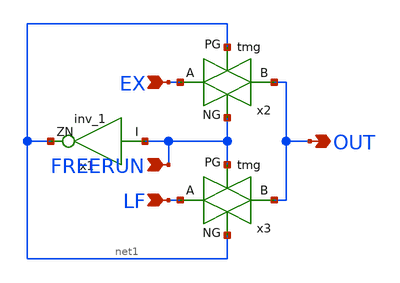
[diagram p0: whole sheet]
** sch_path: ctrlsel.sch
**.subckt ctrlsel OUT EX LF FREERUN
*.opin OUT
*.ipin EX
*.ipin LF
*.ipin FREERUN
x1 FREERUN net1 VDD VDD GND GND gf180mcu_fd_sc_mcu7t5v0__inv_1
x2 net1 OUT EX FREERUN tmg
x3 FREERUN OUT LF net1 tmg
**.ends

* expanding   symbol:  tmg.sym # of pins=4
** sym_path: tmg.sym
** sch_path: tmg.sch
.subckt tmg PG B A NG
*.opin B
*.ipin A
*.ipin PG
*.ipin NG
XM1 B NG A GND nfet_06v0 L=0.70u W=0.30u nf=1 ad='int((nf+1)/2) * W/nf * 0.18u' as='int((nf+2)/2) * W/nf * 0.18u'
+ pd='2*int((nf+1)/2) * (W/nf + 0.18u)' ps='2*int((nf+2)/2) * (W/nf + 0.18u)' nrd='0.18u / W' nrs='0.18u / W'
+ sa=0 sb=0 sd=0 m=1
XM2 A PG B VDD pfet_06v0 L=0.50u W=0.30u nf=1 ad='int((nf+1)/2) * W/nf * 0.18u' as='int((nf+2)/2) * W/nf * 0.18u'
+ pd='2*int((nf+1)/2) * (W/nf + 0.18u)' ps='2*int((nf+2)/2) * (W/nf + 0.18u)' nrd='0.18u / W' nrs='0.18u / W'
+ sa=0 sb=0 sd=0 m=1
.ends

.GLOBAL GND
.GLOBAL VDD
.end
